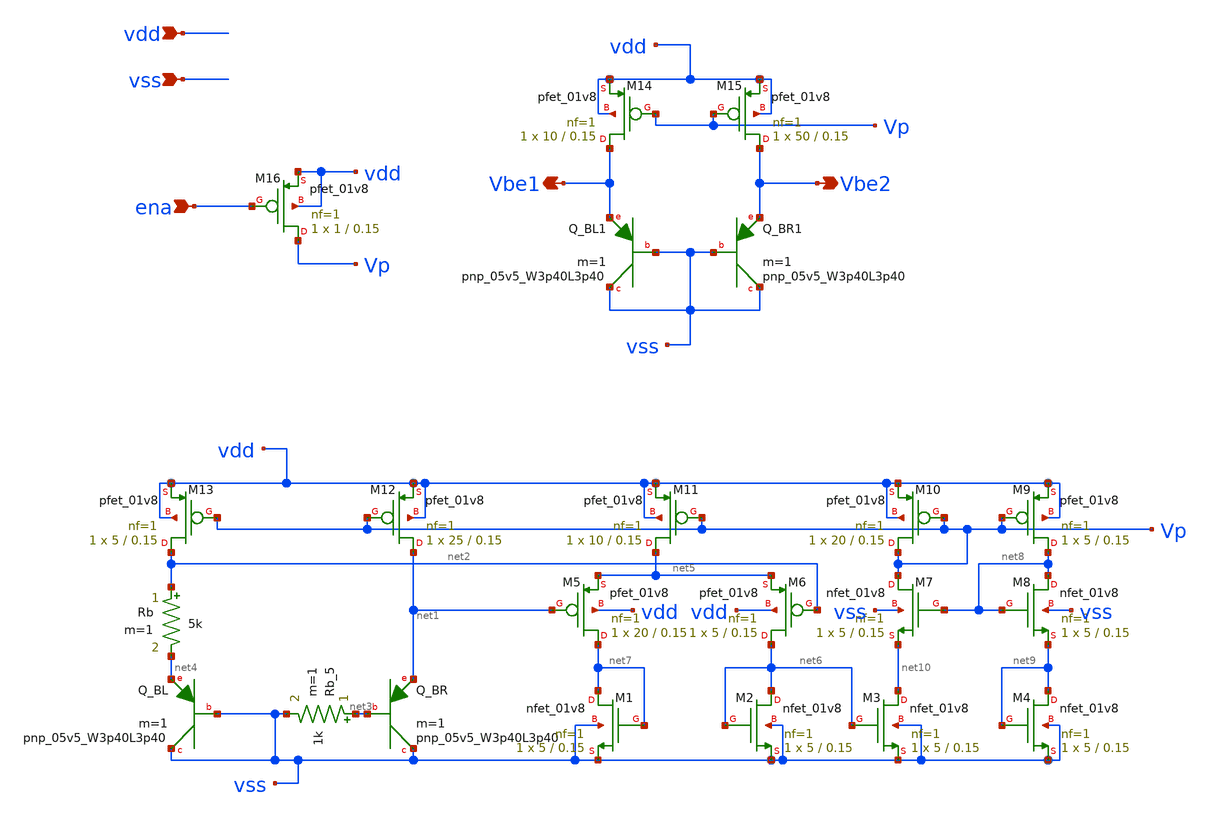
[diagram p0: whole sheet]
** sch_path: xschem/sky130_od_ip__tempsensor.sch
**.subckt sky130_od_ip__tempsensor vdd vss Vbe2 Vbe1 ena
*.ipin vdd
*.ipin vss
*.opin Vbe2
*.opin Vbe1
*.ipin ena
XM12 net1 Vp vdd vdd sky130_fd_pr__pfet_01v8 L=0.15 W=25 nf=1 ad='int((nf+1)/2) * W/nf * 0.29' as='int((nf+2)/2) * W/nf * 0.29'
+ pd='2*int((nf+1)/2) * (W/nf + 0.29)' ps='2*int((nf+2)/2) * (W/nf + 0.29)' nrd='0.29 / W' nrs='0.29 / W'
+ sa=0 sb=0 sd=0 mult=1 m=1
XM13 net2 Vp vdd vdd sky130_fd_pr__pfet_01v8 L=0.15 W=5 nf=1 ad='int((nf+1)/2) * W/nf * 0.29' as='int((nf+2)/2) * W/nf * 0.29'
+ pd='2*int((nf+1)/2) * (W/nf + 0.29)' ps='2*int((nf+2)/2) * (W/nf + 0.29)' nrd='0.29 / W' nrs='0.29 / W'
+ sa=0 sb=0 sd=0 mult=1 m=1
XQ_BR vss net3 net1 sky130_fd_pr__pnp_05v5_W3p40L3p40 m=1
XQ_BL vss vss net4 sky130_fd_pr__pnp_05v5_W3p40L3p40 m=1
Rb net2 net4 5k m=1
Rb_5 net3 vss 1k m=1
XM11 net5 Vp vdd vdd sky130_fd_pr__pfet_01v8 L=0.15 W=10 nf=1 ad='int((nf+1)/2) * W/nf * 0.29' as='int((nf+2)/2) * W/nf * 0.29'
+ pd='2*int((nf+1)/2) * (W/nf + 0.29)' ps='2*int((nf+2)/2) * (W/nf + 0.29)' nrd='0.29 / W' nrs='0.29 / W'
+ sa=0 sb=0 sd=0 mult=1 m=1
XM6 net6 net2 net5 vdd sky130_fd_pr__pfet_01v8 L=0.15 W=5 nf=1 ad='int((nf+1)/2) * W/nf * 0.29' as='int((nf+2)/2) * W/nf * 0.29'
+ pd='2*int((nf+1)/2) * (W/nf + 0.29)' ps='2*int((nf+2)/2) * (W/nf + 0.29)' nrd='0.29 / W' nrs='0.29 / W'
+ sa=0 sb=0 sd=0 mult=1 m=1
XM5 net7 net1 net5 vdd sky130_fd_pr__pfet_01v8 L=0.15 W=20 nf=1 ad='int((nf+1)/2) * W/nf * 0.29' as='int((nf+2)/2) * W/nf * 0.29'
+ pd='2*int((nf+1)/2) * (W/nf + 0.29)' ps='2*int((nf+2)/2) * (W/nf + 0.29)' nrd='0.29 / W' nrs='0.29 / W'
+ sa=0 sb=0 sd=0 mult=1 m=1
XM2 net6 net6 vss vss sky130_fd_pr__nfet_01v8 L=0.15 W=5 nf=1 ad='int((nf+1)/2) * W/nf * 0.29' as='int((nf+2)/2) * W/nf * 0.29'
+ pd='2*int((nf+1)/2) * (W/nf + 0.29)' ps='2*int((nf+2)/2) * (W/nf + 0.29)' nrd='0.29 / W' nrs='0.29 / W'
+ sa=0 sb=0 sd=0 mult=1 m=1
XM1 net7 net7 vss vss sky130_fd_pr__nfet_01v8 L=0.15 W=5 nf=1 ad='int((nf+1)/2) * W/nf * 0.29' as='int((nf+2)/2) * W/nf * 0.29'
+ pd='2*int((nf+1)/2) * (W/nf + 0.29)' ps='2*int((nf+2)/2) * (W/nf + 0.29)' nrd='0.29 / W' nrs='0.29 / W'
+ sa=0 sb=0 sd=0 mult=1 m=1
XM9 net8 Vp vdd vdd sky130_fd_pr__pfet_01v8 L=0.15 W=5 nf=1 ad='int((nf+1)/2) * W/nf * 0.29' as='int((nf+2)/2) * W/nf * 0.29'
+ pd='2*int((nf+1)/2) * (W/nf + 0.29)' ps='2*int((nf+2)/2) * (W/nf + 0.29)' nrd='0.29 / W' nrs='0.29 / W'
+ sa=0 sb=0 sd=0 mult=1 m=1
XM10 Vp Vp vdd vdd sky130_fd_pr__pfet_01v8 L=0.15 W=20 nf=1 ad='int((nf+1)/2) * W/nf * 0.29' as='int((nf+2)/2) * W/nf * 0.29'
+ pd='2*int((nf+1)/2) * (W/nf + 0.29)' ps='2*int((nf+2)/2) * (W/nf + 0.29)' nrd='0.29 / W' nrs='0.29 / W'
+ sa=0 sb=0 sd=0 mult=1 m=1
XM7 Vp net8 net10 vss sky130_fd_pr__nfet_01v8 L=0.15 W=5 nf=1 ad='int((nf+1)/2) * W/nf * 0.29' as='int((nf+2)/2) * W/nf * 0.29'
+ pd='2*int((nf+1)/2) * (W/nf + 0.29)' ps='2*int((nf+2)/2) * (W/nf + 0.29)' nrd='0.29 / W' nrs='0.29 / W'
+ sa=0 sb=0 sd=0 mult=1 m=1
XM8 net8 net8 net9 vss sky130_fd_pr__nfet_01v8 L=0.15 W=5 nf=1 ad='int((nf+1)/2) * W/nf * 0.29' as='int((nf+2)/2) * W/nf * 0.29'
+ pd='2*int((nf+1)/2) * (W/nf + 0.29)' ps='2*int((nf+2)/2) * (W/nf + 0.29)' nrd='0.29 / W' nrs='0.29 / W'
+ sa=0 sb=0 sd=0 mult=1 m=1
XM3 net10 net6 vss vss sky130_fd_pr__nfet_01v8 L=0.15 W=5 nf=1 ad='int((nf+1)/2) * W/nf * 0.29' as='int((nf+2)/2) * W/nf * 0.29'
+ pd='2*int((nf+1)/2) * (W/nf + 0.29)' ps='2*int((nf+2)/2) * (W/nf + 0.29)' nrd='0.29 / W' nrs='0.29 / W'
+ sa=0 sb=0 sd=0 mult=1 m=1
XM4 net9 net9 vss vss sky130_fd_pr__nfet_01v8 L=0.15 W=5 nf=1 ad='int((nf+1)/2) * W/nf * 0.29' as='int((nf+2)/2) * W/nf * 0.29'
+ pd='2*int((nf+1)/2) * (W/nf + 0.29)' ps='2*int((nf+2)/2) * (W/nf + 0.29)' nrd='0.29 / W' nrs='0.29 / W'
+ sa=0 sb=0 sd=0 mult=1 m=1
XQ_BL1 vss vss Vbe1 sky130_fd_pr__pnp_05v5_W3p40L3p40 m=1
XQ_BR1 vss vss Vbe2 sky130_fd_pr__pnp_05v5_W3p40L3p40 m=1
XM14 Vbe1 Vp vdd vdd sky130_fd_pr__pfet_01v8 L=0.15 W=10 nf=1 ad='int((nf+1)/2) * W/nf * 0.29' as='int((nf+2)/2) * W/nf * 0.29'
+ pd='2*int((nf+1)/2) * (W/nf + 0.29)' ps='2*int((nf+2)/2) * (W/nf + 0.29)' nrd='0.29 / W' nrs='0.29 / W'
+ sa=0 sb=0 sd=0 mult=1 m=1
XM15 Vbe2 Vp vdd vdd sky130_fd_pr__pfet_01v8 L=0.15 W=50 nf=1 ad='int((nf+1)/2) * W/nf * 0.29' as='int((nf+2)/2) * W/nf * 0.29'
+ pd='2*int((nf+1)/2) * (W/nf + 0.29)' ps='2*int((nf+2)/2) * (W/nf + 0.29)' nrd='0.29 / W' nrs='0.29 / W'
+ sa=0 sb=0 sd=0 mult=1 m=1
XM16 Vp ena vdd vdd sky130_fd_pr__pfet_01v8 L=0.15 W=1 nf=1 ad='int((nf+1)/2) * W/nf * 0.29' as='int((nf+2)/2) * W/nf * 0.29'
+ pd='2*int((nf+1)/2) * (W/nf + 0.29)' ps='2*int((nf+2)/2) * (W/nf + 0.29)' nrd='0.29 / W' nrs='0.29 / W'
+ sa=0 sb=0 sd=0 mult=1 m=1
**.ends
.end
